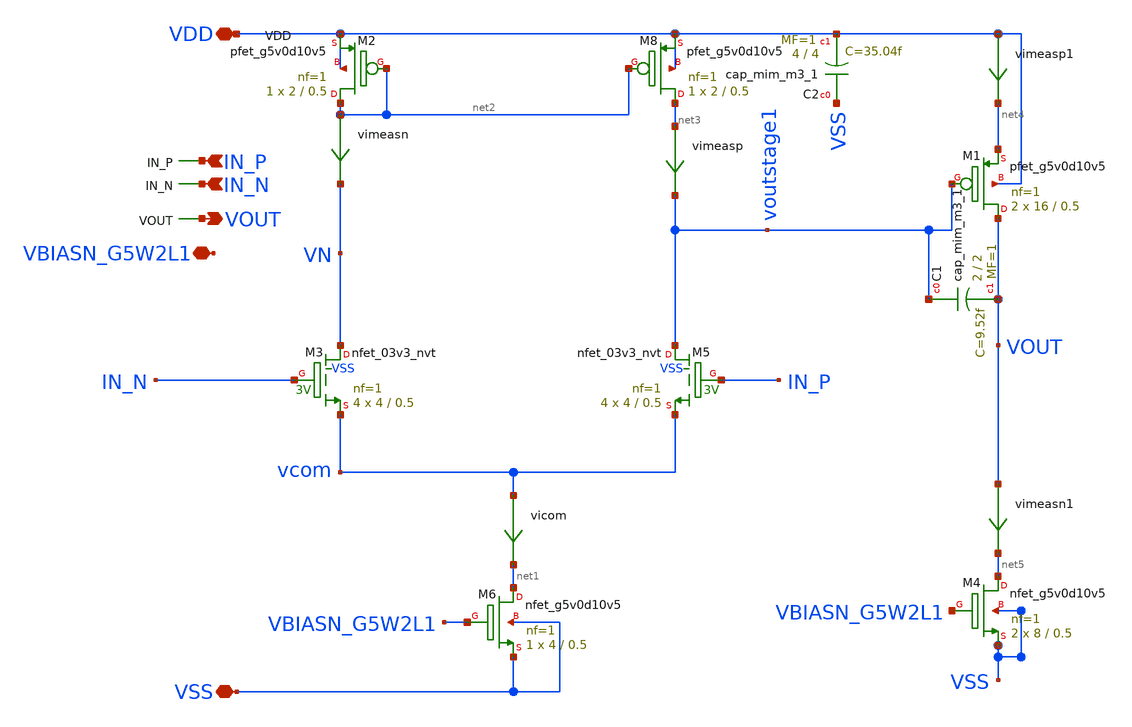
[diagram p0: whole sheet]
** sch_path: xschem/opamp3hv.sch
**.subckt opamp3hv IN_N IN_P VOUT VDD VSS VBIASN_G5W2L1
*.ipin IN_N
*.ipin IN_P
*.opin VOUT
*.iopin VDD
*.iopin VSS
*.iopin VBIASN_G5W2L1
vimeasp net3 voutstage1 0
.save i(vimeasp)
vimeasn net2 VN 0
.save i(vimeasn)
XC1 voutstage1 VOUT sky130_fd_pr__cap_mim_m3_1 W=2 L=2 MF=1 m=1
XM6 net1 VBIASN_G5W2L1 VSS VSS sky130_fd_pr__nfet_g5v0d10v5 L=0.5 W=4 nf=1 ad='int((nf+1)/2) * W/nf * 0.29'
+ as='int((nf+2)/2) * W/nf * 0.29' pd='2*int((nf+1)/2) * (W/nf + 0.29)' ps='2*int((nf+2)/2) * (W/nf + 0.29)'
+ nrd='0.29 / W' nrs='0.29 / W' sa=0 sb=0 sd=0 mult=1 m=1
XM8 net3 net2 VDD VDD sky130_fd_pr__pfet_g5v0d10v5 L=0.5 W=2 nf=1 ad='int((nf+1)/2) * W/nf * 0.29' as='int((nf+2)/2) * W/nf * 0.29'
+ pd='2*int((nf+1)/2) * (W/nf + 0.29)' ps='2*int((nf+2)/2) * (W/nf + 0.29)' nrd='0.29 / W' nrs='0.29 / W'
+ sa=0 sb=0 sd=0 mult=1 m=1
XM2 net2 net2 VDD VDD sky130_fd_pr__pfet_g5v0d10v5 L=0.5 W=2 nf=1 ad='int((nf+1)/2) * W/nf * 0.29' as='int((nf+2)/2) * W/nf * 0.29'
+ pd='2*int((nf+1)/2) * (W/nf + 0.29)' ps='2*int((nf+2)/2) * (W/nf + 0.29)' nrd='0.29 / W' nrs='0.29 / W'
+ sa=0 sb=0 sd=0 mult=1 m=1
XM1 VOUT voutstage1 net4 VDD sky130_fd_pr__pfet_g5v0d10v5 L=0.5 W=16 nf=1 ad='int((nf+1)/2) * W/nf * 0.29'
+ as='int((nf+2)/2) * W/nf * 0.29' pd='2*int((nf+1)/2) * (W/nf + 0.29)' ps='2*int((nf+2)/2) * (W/nf + 0.29)'
+ nrd='0.29 / W' nrs='0.29 / W' sa=0 sb=0 sd=0 mult=2 m=2
XM4 net5 VBIASN_G5W2L1 VSS VSS sky130_fd_pr__nfet_g5v0d10v5 L=0.5 W=8 nf=1 ad='int((nf+1)/2) * W/nf * 0.29'
+ as='int((nf+2)/2) * W/nf * 0.29' pd='2*int((nf+1)/2) * (W/nf + 0.29)' ps='2*int((nf+2)/2) * (W/nf + 0.29)'
+ nrd='0.29 / W' nrs='0.29 / W' sa=0 sb=0 sd=0 mult=2 m=2
XM3 VN IN_N vcom VSS sky130_fd_pr__nfet_03v3_nvt L=0.5 W=4 nf=1 ad='int((nf+1)/2) * W/nf * 0.29' as='int((nf+2)/2) * W/nf * 0.29'
+ pd='2*int((nf+1)/2) * (W/nf + 0.29)' ps='2*int((nf+2)/2) * (W/nf + 0.29)' nrd='0.29 / W' nrs='0.29 / W'
+ sa=0 sb=0 sd=0 mult=4 m=4
XM5 voutstage1 IN_P vcom VSS sky130_fd_pr__nfet_03v3_nvt L=0.5 W=4 nf=1 ad='int((nf+1)/2) * W/nf * 0.29'
+ as='int((nf+2)/2) * W/nf * 0.29' pd='2*int((nf+1)/2) * (W/nf + 0.29)' ps='2*int((nf+2)/2) * (W/nf + 0.29)'
+ nrd='0.29 / W' nrs='0.29 / W' sa=0 sb=0 sd=0 mult=4 m=4
vicom vcom net1 0
.save i(vicom)
XC2 VSS VDD sky130_fd_pr__cap_mim_m3_1 W=4 L=4 MF=1 m=1
vimeasp1 VDD net4 0
.save i(vimeasp1)
vimeasn1 VOUT net5 0
.save i(vimeasn1)
**.ends
.end
